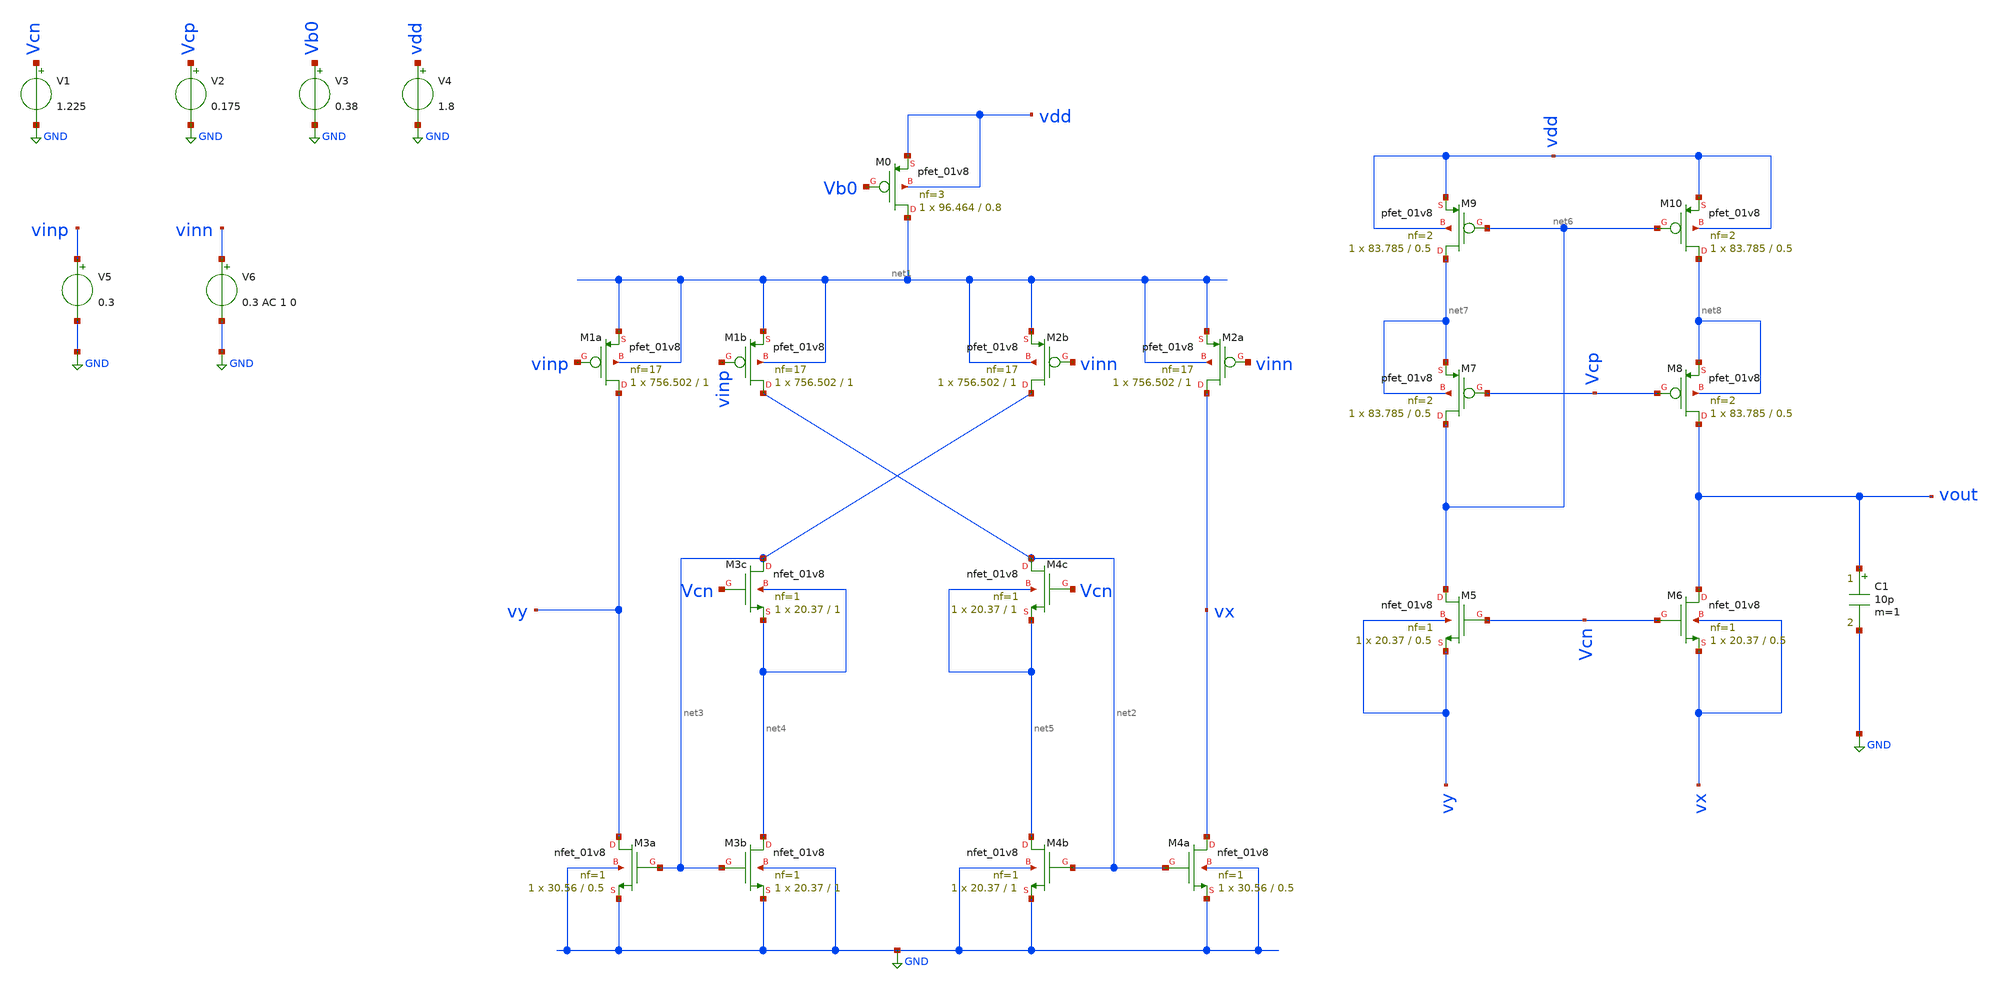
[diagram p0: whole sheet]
** sch_path: CASS2.sch
**.subckt CASS2
XM3c net3 Vcn net4 net4 sky130_fd_pr__nfet_01v8 L=1 W=20.37 nf=1 ad='int((nf+1)/2) * W/nf * 0.29' as='int((nf+2)/2) * W/nf * 0.29'
+ pd='2*int((nf+1)/2) * (W/nf + 0.29)' ps='2*int((nf+2)/2) * (W/nf + 0.29)' nrd='0.29 / W' nrs='0.29 / W'
+ sa=0 sb=0 sd=0 mult=1 m=1
XM4c net2 Vcn net5 net5 sky130_fd_pr__nfet_01v8 L=1 W=20.37 nf=1 ad='int((nf+1)/2) * W/nf * 0.29' as='int((nf+2)/2) * W/nf * 0.29'
+ pd='2*int((nf+1)/2) * (W/nf + 0.29)' ps='2*int((nf+2)/2) * (W/nf + 0.29)' nrd='0.29 / W' nrs='0.29 / W'
+ sa=0 sb=0 sd=0 mult=1 m=1
XM3b net4 net3 GND GND sky130_fd_pr__nfet_01v8 L=1 W=20.37 nf=1 ad='int((nf+1)/2) * W/nf * 0.29' as='int((nf+2)/2) * W/nf * 0.29'
+ pd='2*int((nf+1)/2) * (W/nf + 0.29)' ps='2*int((nf+2)/2) * (W/nf + 0.29)' nrd='0.29 / W' nrs='0.29 / W'
+ sa=0 sb=0 sd=0 mult=1 m=1
XM4b net5 net2 GND GND sky130_fd_pr__nfet_01v8 L=1 W=20.37 nf=1 ad='int((nf+1)/2) * W/nf * 0.29' as='int((nf+2)/2) * W/nf * 0.29'
+ pd='2*int((nf+1)/2) * (W/nf + 0.29)' ps='2*int((nf+2)/2) * (W/nf + 0.29)' nrd='0.29 / W' nrs='0.29 / W'
+ sa=0 sb=0 sd=0 mult=1 m=1
XM3a vy net3 GND GND sky130_fd_pr__nfet_01v8 L=0.5 W=30.56 nf=1 ad='int((nf+1)/2) * W/nf * 0.29' as='int((nf+2)/2) * W/nf * 0.29'
+ pd='2*int((nf+1)/2) * (W/nf + 0.29)' ps='2*int((nf+2)/2) * (W/nf + 0.29)' nrd='0.29 / W' nrs='0.29 / W'
+ sa=0 sb=0 sd=0 mult=1 m=1
XM4a vx net2 GND GND sky130_fd_pr__nfet_01v8 L=0.5 W=30.56 nf=1 ad='int((nf+1)/2) * W/nf * 0.29' as='int((nf+2)/2) * W/nf * 0.29'
+ pd='2*int((nf+1)/2) * (W/nf + 0.29)' ps='2*int((nf+2)/2) * (W/nf + 0.29)' nrd='0.29 / W' nrs='0.29 / W'
+ sa=0 sb=0 sd=0 mult=1 m=1
XM2b net3 vinn net1 net1 sky130_fd_pr__pfet_01v8 L=1 W=756.502 nf=17 ad='int((nf+1)/2) * W/nf * 0.29'
+ as='int((nf+2)/2) * W/nf * 0.29' pd='2*int((nf+1)/2) * (W/nf + 0.29)' ps='2*int((nf+2)/2) * (W/nf + 0.29)'
+ nrd='0.29 / W' nrs='0.29 / W' sa=0 sb=0 sd=0 mult=1 m=1
XM2a vx vinn net1 net1 sky130_fd_pr__pfet_01v8 L=1 W=756.502 nf=17 ad='int((nf+1)/2) * W/nf * 0.29' as='int((nf+2)/2) * W/nf * 0.29'
+ pd='2*int((nf+1)/2) * (W/nf + 0.29)' ps='2*int((nf+2)/2) * (W/nf + 0.29)' nrd='0.29 / W' nrs='0.29 / W'
+ sa=0 sb=0 sd=0 mult=1 m=1
XM1b net2 vinp net1 net1 sky130_fd_pr__pfet_01v8 L=1 W=756.502 nf=17 ad='int((nf+1)/2) * W/nf * 0.29'
+ as='int((nf+2)/2) * W/nf * 0.29' pd='2*int((nf+1)/2) * (W/nf + 0.29)' ps='2*int((nf+2)/2) * (W/nf + 0.29)'
+ nrd='0.29 / W' nrs='0.29 / W' sa=0 sb=0 sd=0 mult=1 m=1
XM1a vy vinp net1 net1 sky130_fd_pr__pfet_01v8 L=1 W=756.502 nf=17 ad='int((nf+1)/2) * W/nf * 0.29' as='int((nf+2)/2) * W/nf * 0.29'
+ pd='2*int((nf+1)/2) * (W/nf + 0.29)' ps='2*int((nf+2)/2) * (W/nf + 0.29)' nrd='0.29 / W' nrs='0.29 / W'
+ sa=0 sb=0 sd=0 mult=1 m=1
XM0 net1 Vb0 vdd vdd sky130_fd_pr__pfet_01v8 L=0.8 W=96.464 nf=3 ad='int((nf+1)/2) * W/nf * 0.29' as='int((nf+2)/2) * W/nf * 0.29'
+ pd='2*int((nf+1)/2) * (W/nf + 0.29)' ps='2*int((nf+2)/2) * (W/nf + 0.29)' nrd='0.29 / W' nrs='0.29 / W'
+ sa=0 sb=0 sd=0 mult=1 m=1
XM6 vout Vcn vx vx sky130_fd_pr__nfet_01v8 L=0.5 W=20.37 nf=1 ad='int((nf+1)/2) * W/nf * 0.29' as='int((nf+2)/2) * W/nf * 0.29'
+ pd='2*int((nf+1)/2) * (W/nf + 0.29)' ps='2*int((nf+2)/2) * (W/nf + 0.29)' nrd='0.29 / W' nrs='0.29 / W'
+ sa=0 sb=0 sd=0 mult=1 m=1
XM5 net6 Vcn vy vy sky130_fd_pr__nfet_01v8 L=0.5 W=20.37 nf=1 ad='int((nf+1)/2) * W/nf * 0.29' as='int((nf+2)/2) * W/nf * 0.29'
+ pd='2*int((nf+1)/2) * (W/nf + 0.29)' ps='2*int((nf+2)/2) * (W/nf + 0.29)' nrd='0.29 / W' nrs='0.29 / W'
+ sa=0 sb=0 sd=0 mult=1 m=1
XM10 net8 net6 vdd vdd sky130_fd_pr__pfet_01v8 L=0.5 W=83.785 nf=2 ad='int((nf+1)/2) * W/nf * 0.29' as='int((nf+2)/2) * W/nf * 0.29'
+ pd='2*int((nf+1)/2) * (W/nf + 0.29)' ps='2*int((nf+2)/2) * (W/nf + 0.29)' nrd='0.29 / W' nrs='0.29 / W'
+ sa=0 sb=0 sd=0 mult=1 m=1
XM9 net7 net6 vdd vdd sky130_fd_pr__pfet_01v8 L=0.5 W=83.785 nf=2 ad='int((nf+1)/2) * W/nf * 0.29' as='int((nf+2)/2) * W/nf * 0.29'
+ pd='2*int((nf+1)/2) * (W/nf + 0.29)' ps='2*int((nf+2)/2) * (W/nf + 0.29)' nrd='0.29 / W' nrs='0.29 / W'
+ sa=0 sb=0 sd=0 mult=1 m=1
XM8 vout Vcp net8 net8 sky130_fd_pr__pfet_01v8 L=0.5 W=83.785 nf=2 ad='int((nf+1)/2) * W/nf * 0.29' as='int((nf+2)/2) * W/nf * 0.29'
+ pd='2*int((nf+1)/2) * (W/nf + 0.29)' ps='2*int((nf+2)/2) * (W/nf + 0.29)' nrd='0.29 / W' nrs='0.29 / W'
+ sa=0 sb=0 sd=0 mult=1 m=1
XM7 net6 Vcp net7 net7 sky130_fd_pr__pfet_01v8 L=0.5 W=83.785 nf=2 ad='int((nf+1)/2) * W/nf * 0.29' as='int((nf+2)/2) * W/nf * 0.29'
+ pd='2*int((nf+1)/2) * (W/nf + 0.29)' ps='2*int((nf+2)/2) * (W/nf + 0.29)' nrd='0.29 / W' nrs='0.29 / W'
+ sa=0 sb=0 sd=0 mult=1 m=1
C1 vout GND 10p m=1
V1 Vcn GND 1.225
V2 Vcp GND 0.175
V3 Vb0 GND 0.38
V4 vdd GND 1.8
V5 vinp GND 0.3
V6 vinn GND 0.3 AC 1 0
**** begin user architecture code



*.op
*.tran 10ns 1us
.options savecurrents
.save all @m.xm1a.msky130_fd_pr__pfet_01v8[id]  @m.xm0.msky130_fd_pr__pfet_01v8[gm] @m.xm1a.msky130_fd_pr__pfet_01v8[gm] @m.xm2a.msky130_fd_pr__pfet_01v8[gm] @m.xm2b.msky130_fd_pr__pfet_01v8[gm]  @m.xm3a.msky130_fd_pr__nfet_01v8[gm] @m.xm3b.msky130_fd_pr__nfet_01v8[gm] @m.xm3c.msky130_fd_pr__nfet_01v8[gm]  @m.xm4a.msky130_fd_pr__nfet_01v8[gm] @m.xm4b.msky130_fd_pr__nfet_01v8[gm] @m.xm4c.msky130_fd_pr__nfet_01v8[gm]  @m.xm5.msky130_fd_pr__nfet_01v8[gm] @m.xm6.msky130_fd_pr__nfet_01v8[gm] @m.xm7.msky130_fd_pr__pfet_01v8[gm] @m.xm8.msky130_fd_pr__pfet_01v8[gm]  @m.xm9.msky130_fd_pr__pfet_01v8[gm] @m.xm10.msky130_fd_pr__pfet_01v8[gm] @m.xm0.msky130_fd_pr__pfet_01v8[vds]  @m.xm1a.msky130_fd_pr__pfet_01v8[vds] @m.xm1b.msky130_fd_pr__pfet_01v8[vds] @m.xm2a.msky130_fd_pr__pfet_01v8[vds]  @m.xm2b.msky130_fd_pr__pfet_01v8[vds] @m.xm3a.msky130_fd_pr__nfet_01v8[vds] @m.xm3b.msky130_fd_pr__nfet_01v8[vds]  @m.xm3c.msky130_fd_pr__nfet_01v8[vds] @m.xm4a.msky130_fd_pr__nfet_01v8[vds] @m.xm4b.msky130_fd_pr__nfet_01v8[vds]  @m.xm4c.msky130_fd_pr__nfet_01v8[vds] @m.xm5.msky130_fd_pr__nfet_01v8[vds] @m.xm6.msky130_fd_pr__nfet_01v8[vds]  @m.xm7.msky130_fd_pr__pfet_01v8[vds] @m.xm8.msky130_fd_pr__pfet_01v8[vds] @m.xm9.msky130_fd_pr__pfet_01v8[vds]  @m.xm10.msky130_fd_pr__pfet_01v8[vds] @m.xm0.msky130_fd_pr__pfet_01v8[vdsat] @m.xm1a.msky130_fd_pr__pfet_01v8[vdsat]  @m.xm1b.msky130_fd_pr__pfet_01v8[vdsat] @m.xm2a.msky130_fd_pr__pfet_01v8[vdsat] @m.xm2b.msky130_fd_pr__pfet_01v8[vdsat]  @m.xm3a.msky130_fd_pr__nfet_01v8[vdsat] @m.xm3b.msky130_fd_pr__nfet_01v8[vdsat] @m.xm3c.msky130_fd_pr__nfet_01v8[vdsat]  @m.xm4a.msky130_fd_pr__nfet_01v8[vdsat] @m.xm4b.msky130_fd_pr__nfet_01v8[vdsat] @m.xm4c.msky130_fd_pr__nfet_01v8[vdsat] @m.xm5.msky130_fd_pr__nfet_01v8[vdsat] @m.xm6.msky130_fd_pr__nfet_01v8[vdsat] @m.xm7.msky130_fd_pr__pfet_01v8[vdsat]  @m.xm8.msky130_fd_pr__pfet_01v8[vdsat] @m.xm9.msky130_fd_pr__pfet_01v8[vdsat] @m.xm10.msky130_fd_pr__pfet_01v8[vdsat]  @m.xm1a.msky130_fd_pr__pfet_01v8[vth] @m.xm1b.msky130_fd_pr__pfet_01v8[vth] @m.xm2a.msky130_fd_pr__pfet_01v8[vth] @m.xm2b.msky130_fd_pr__pfet_01v8[vth] @m.xm3a.msky130_fd_pr__nfet_01v8[vth] @m.xm3b.msky130_fd_pr__nfet_01v8[vth]  @m.xm3c.msky130_fd_pr__nfet_01v8[vth] @m.xm4a.msky130_fd_pr__nfet_01v8[vth] @m.xm4b.msky130_fd_pr__nfet_01v8[vth] @m.xm4c.msky130_fd_pr__nfet_01v8[vth] @m.xm5.msky130_fd_pr__nfet_01v8[vth] @m.xm6.msky130_fd_pr__nfet_01v8[vth]  @m.xm7.msky130_fd_pr__pfet_01v8[vth] @m.xm8.msky130_fd_pr__pfet_01v8[vth] @m.xm9.msky130_fd_pr__pfet_01v8[vth]  @m.xm10.msky130_fd_pr__pfet_01v8[vth] @m.xm0.msky130_fd_pr__pfet_01v8[vth] @m.xm1b.msky130_fd_pr__pfet_01v8[gm]

.control
*op
ac dec 10 100 1000Meg
set units = degrees
run
remzerovec
*plot vdb(vout) ph(vout)
*tran 0.1 20m 10n
*plot v(vout) v(vinn)
write CASS2.raw

set appendwrite
op
print @m.xm1a.msky130_fd_pr__pfet_01v8[id]
print @m.xm1a.msky130_fd_pr__pfet_01v8[gm]
print @m.xm1a.msky130_fd_pr__pfet_01v8[vth]
print @m.xm1a.msky130_fd_pr__pfet_01v8[vdsat]
write CASS2.raw

*set appendwrite
*tran 10ns 100us
*write CASS2.raw
.endc




** opencircuitdesign pdks install
.lib $::SKYWATER_MODELS/sky130.lib.spice tt


**** end user architecture code
**.ends
.GLOBAL GND
.end
